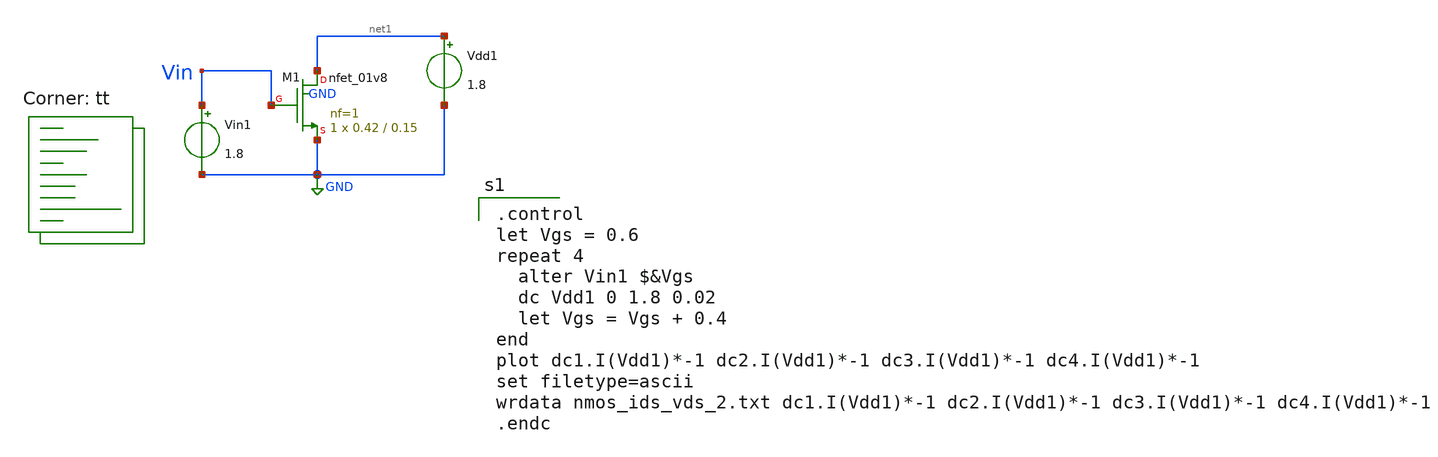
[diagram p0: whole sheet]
** sch_path: tut1/nmos/obsolete/tut1-expt2.sch
**.subckt tut1-expt2
Vin1 Vin GND 1.8
Vdd1 net1 GND 1.8
XM1 net1 Vin GND GND sky130_fd_pr__nfet_01v8 L=0.15 W=0.42 nf=1 ad='int((nf+1)/2) * W/nf * 0.29' as='int((nf+2)/2) * W/nf * 0.29'
+ pd='2*int((nf+1)/2) * (W/nf + 0.29)' ps='2*int((nf+2)/2) * (W/nf + 0.29)' nrd='0.29 / W' nrs='0.29 / W'
+ sa=0 sb=0 sd=0 mult=1 m=1
**** begin user architecture code
.lib $::SKYWATER_MODELS/sky130.lib.spice tt

.control
let Vgs = 0.6
repeat 4
  alter Vin1 $&Vgs
  dc Vdd1 0 1.8 0.02
  let Vgs = Vgs + 0.4
end
plot dc1.I(Vdd1)*-1 dc2.I(Vdd1)*-1 dc3.I(Vdd1)*-1 dc4.I(Vdd1)*-1
set filetype=ascii
wrdata nmos_ids_vds_2.txt dc1.I(Vdd1)*-1 dc2.I(Vdd1)*-1 dc3.I(Vdd1)*-1 dc4.I(Vdd1)*-1
.endc


**** end user architecture code
**.ends
.GLOBAL GND
.end
